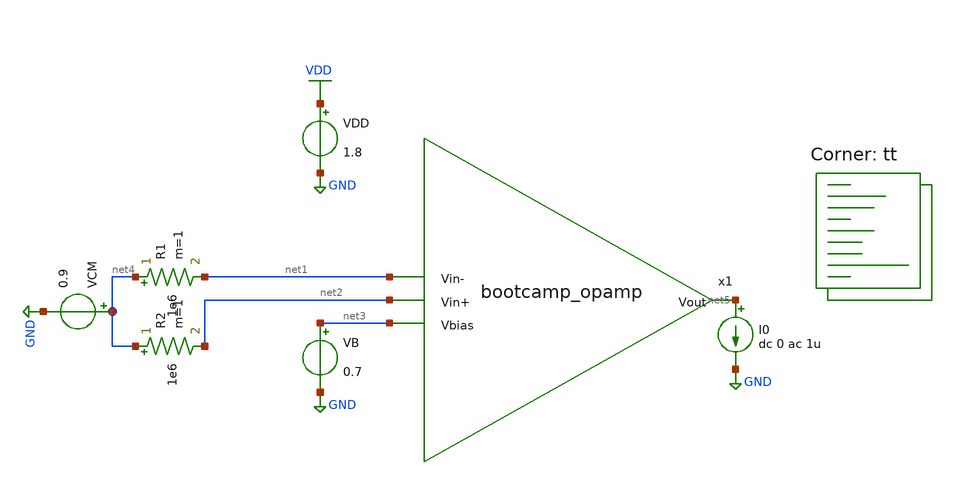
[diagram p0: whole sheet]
** sch_path: analog/schematics/tb_impedance.sch
**.subckt tb_impedance
x1 net5 net1 net2 net3 bootcamp_opamp
VDD VDD GND 1.8
VCM net4 GND 0.9
VB net3 GND 0.7
R1 net4 net1 1e6 m=1
R2 net4 net2 1e6 m=1
I0 net5 GND dc 0 ac 1u
**** begin user architecture code
.lib $::SKYWATER_MODELS/sky130.lib.spice tt
**** end user architecture code
**.ends
.GLOBAL GND
.GLOBAL VDD
.end
